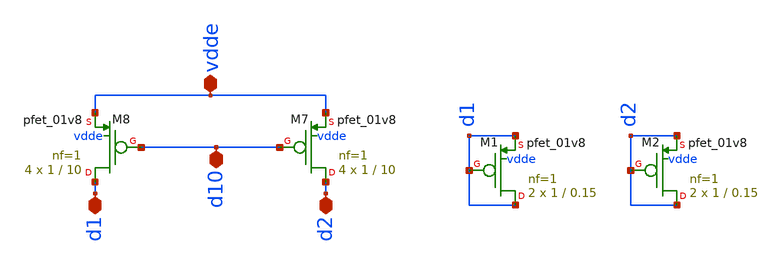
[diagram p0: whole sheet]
** sch_path: magic/pmos_current_bgr.sch
**.subckt pmos_current_bgr d10 d2 d1 vdde
*.iopin d10
*.iopin d2
*.iopin d1
*.iopin vdde
XM7 d2 d10 vdde vdde sky130_fd_pr__pfet_01v8 L=10 W=1 nf=1 ad='int((nf+1)/2) * W/nf * 0.29' as='int((nf+2)/2) * W/nf * 0.29'
+ pd='2*int((nf+1)/2) * (W/nf + 0.29)' ps='2*int((nf+2)/2) * (W/nf + 0.29)' nrd='0.29 / W' nrs='0.29 / W'
+ sa=0 sb=0 sd=0 mult=4 m=4
XM8 d1 d10 vdde vdde sky130_fd_pr__pfet_01v8 L=10 W=1 nf=1 ad='int((nf+1)/2) * W/nf * 0.29' as='int((nf+2)/2) * W/nf * 0.29'
+ pd='2*int((nf+1)/2) * (W/nf + 0.29)' ps='2*int((nf+2)/2) * (W/nf + 0.29)' nrd='0.29 / W' nrs='0.29 / W'
+ sa=0 sb=0 sd=0 mult=4 m=4
XM1 d1 d1 d1 vdde sky130_fd_pr__pfet_01v8 L=0.15 W=1 nf=1 ad='int((nf+1)/2) * W/nf * 0.29' as='int((nf+2)/2) * W/nf * 0.29'
+ pd='2*int((nf+1)/2) * (W/nf + 0.29)' ps='2*int((nf+2)/2) * (W/nf + 0.29)' nrd='0.29 / W' nrs='0.29 / W'
+ sa=0 sb=0 sd=0 mult=2 m=2
XM2 d2 d2 d2 vdde sky130_fd_pr__pfet_01v8 L=0.15 W=1 nf=1 ad='int((nf+1)/2) * W/nf * 0.29' as='int((nf+2)/2) * W/nf * 0.29'
+ pd='2*int((nf+1)/2) * (W/nf + 0.29)' ps='2*int((nf+2)/2) * (W/nf + 0.29)' nrd='0.29 / W' nrs='0.29 / W'
+ sa=0 sb=0 sd=0 mult=2 m=2
**.ends
.end
